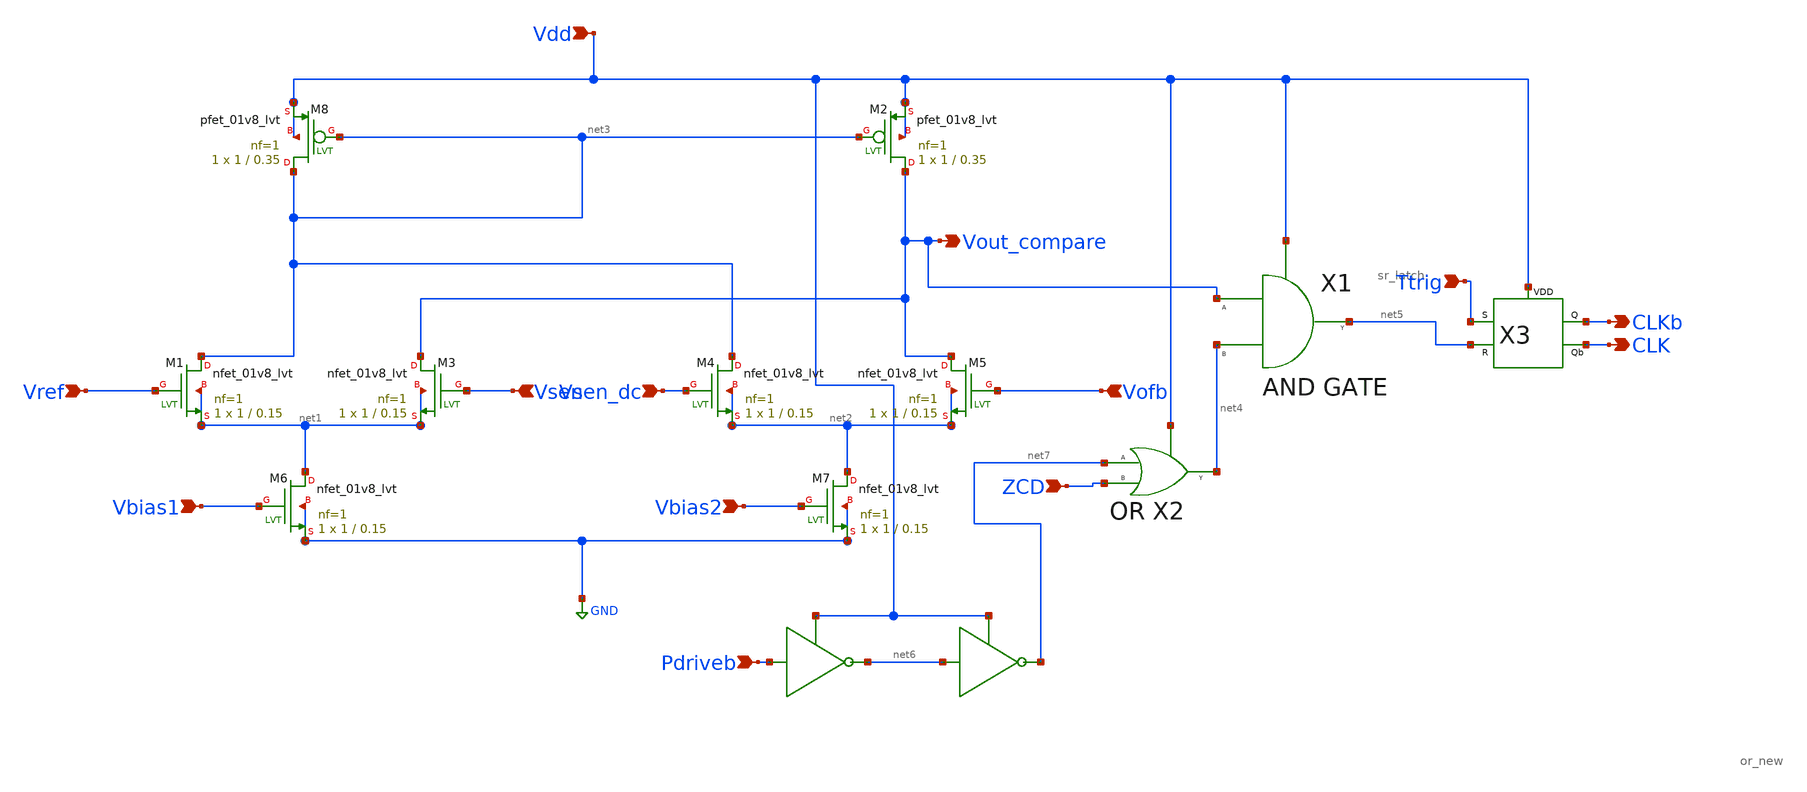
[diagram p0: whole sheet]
** sch_path: Current Sensor/mroat.sch
**.subckt mroat Vref Vsen_dc Vofb Vsen Vbias1 Vbias2 Vdd Vout_compare CLKb CLK Ttrig Pdriveb ZCD
*.ipin Vref
*.ipin Vsen_dc
*.ipin Vofb
*.ipin Vsen
*.ipin Vbias1
*.ipin Vbias2
*.ipin Vdd
*.opin Vout_compare
*.opin CLKb
*.opin CLK
*.ipin Ttrig
*.ipin Pdriveb
*.ipin ZCD
XM1 net3 Vref net1 net1 sky130_fd_pr__nfet_01v8_lvt L=0.15 W=1 nf=1 ad='int((nf+1)/2) * W/nf * 0.29'
+ as='int((nf+2)/2) * W/nf * 0.29' pd='2*int((nf+1)/2) * (W/nf + 0.29)' ps='2*int((nf+2)/2) * (W/nf + 0.29)'
+ nrd='0.29 / W' nrs='0.29 / W' sa=0 sb=0 sd=0 mult=1 m=1
XM2 Vout_compare net3 Vdd Vdd sky130_fd_pr__pfet_01v8_lvt L=0.35 W=1 nf=1 ad='int((nf+1)/2) * W/nf * 0.29'
+ as='int((nf+2)/2) * W/nf * 0.29' pd='2*int((nf+1)/2) * (W/nf + 0.29)' ps='2*int((nf+2)/2) * (W/nf + 0.29)'
+ nrd='0.29 / W' nrs='0.29 / W' sa=0 sb=0 sd=0 mult=1 m=1
XM3 Vout_compare Vsen net1 net1 sky130_fd_pr__nfet_01v8_lvt L=0.15 W=1 nf=1 ad='int((nf+1)/2) * W/nf * 0.29'
+ as='int((nf+2)/2) * W/nf * 0.29' pd='2*int((nf+1)/2) * (W/nf + 0.29)' ps='2*int((nf+2)/2) * (W/nf + 0.29)'
+ nrd='0.29 / W' nrs='0.29 / W' sa=0 sb=0 sd=0 mult=1 m=1
XM4 net3 Vsen_dc net2 net2 sky130_fd_pr__nfet_01v8_lvt L=0.15 W=1 nf=1 ad='int((nf+1)/2) * W/nf * 0.29'
+ as='int((nf+2)/2) * W/nf * 0.29' pd='2*int((nf+1)/2) * (W/nf + 0.29)' ps='2*int((nf+2)/2) * (W/nf + 0.29)'
+ nrd='0.29 / W' nrs='0.29 / W' sa=0 sb=0 sd=0 mult=1 m=1
XM5 Vout_compare Vofb net2 net2 sky130_fd_pr__nfet_01v8_lvt L=0.15 W=1 nf=1 ad='int((nf+1)/2) * W/nf * 0.29'
+ as='int((nf+2)/2) * W/nf * 0.29' pd='2*int((nf+1)/2) * (W/nf + 0.29)' ps='2*int((nf+2)/2) * (W/nf + 0.29)'
+ nrd='0.29 / W' nrs='0.29 / W' sa=0 sb=0 sd=0 mult=1 m=1
XM6 net1 Vbias1 GND GND sky130_fd_pr__nfet_01v8_lvt L=0.15 W=1 nf=1 ad='int((nf+1)/2) * W/nf * 0.29'
+ as='int((nf+2)/2) * W/nf * 0.29' pd='2*int((nf+1)/2) * (W/nf + 0.29)' ps='2*int((nf+2)/2) * (W/nf + 0.29)'
+ nrd='0.29 / W' nrs='0.29 / W' sa=0 sb=0 sd=0 mult=1 m=1
XM7 net2 Vbias2 GND GND sky130_fd_pr__nfet_01v8_lvt L=0.15 W=1 nf=1 ad='int((nf+1)/2) * W/nf * 0.29'
+ as='int((nf+2)/2) * W/nf * 0.29' pd='2*int((nf+1)/2) * (W/nf + 0.29)' ps='2*int((nf+2)/2) * (W/nf + 0.29)'
+ nrd='0.29 / W' nrs='0.29 / W' sa=0 sb=0 sd=0 mult=1 m=1
XM8 net3 net3 Vdd Vdd sky130_fd_pr__pfet_01v8_lvt L=0.35 W=1 nf=1 ad='int((nf+1)/2) * W/nf * 0.29' as='int((nf+2)/2) * W/nf * 0.29'
+ pd='2*int((nf+1)/2) * (W/nf + 0.29)' ps='2*int((nf+2)/2) * (W/nf + 0.29)' nrd='0.29 / W' nrs='0.29 / W'
+ sa=0 sb=0 sd=0 mult=1 m=1
X1 Vout_compare net4 net5 Vdd and
X3 Ttrig net5 CLKb CLK Vdd sr_latch
X2 ZCD net7 net4 Vdd or_new
**.ends
.GLOBAL GND
.end
